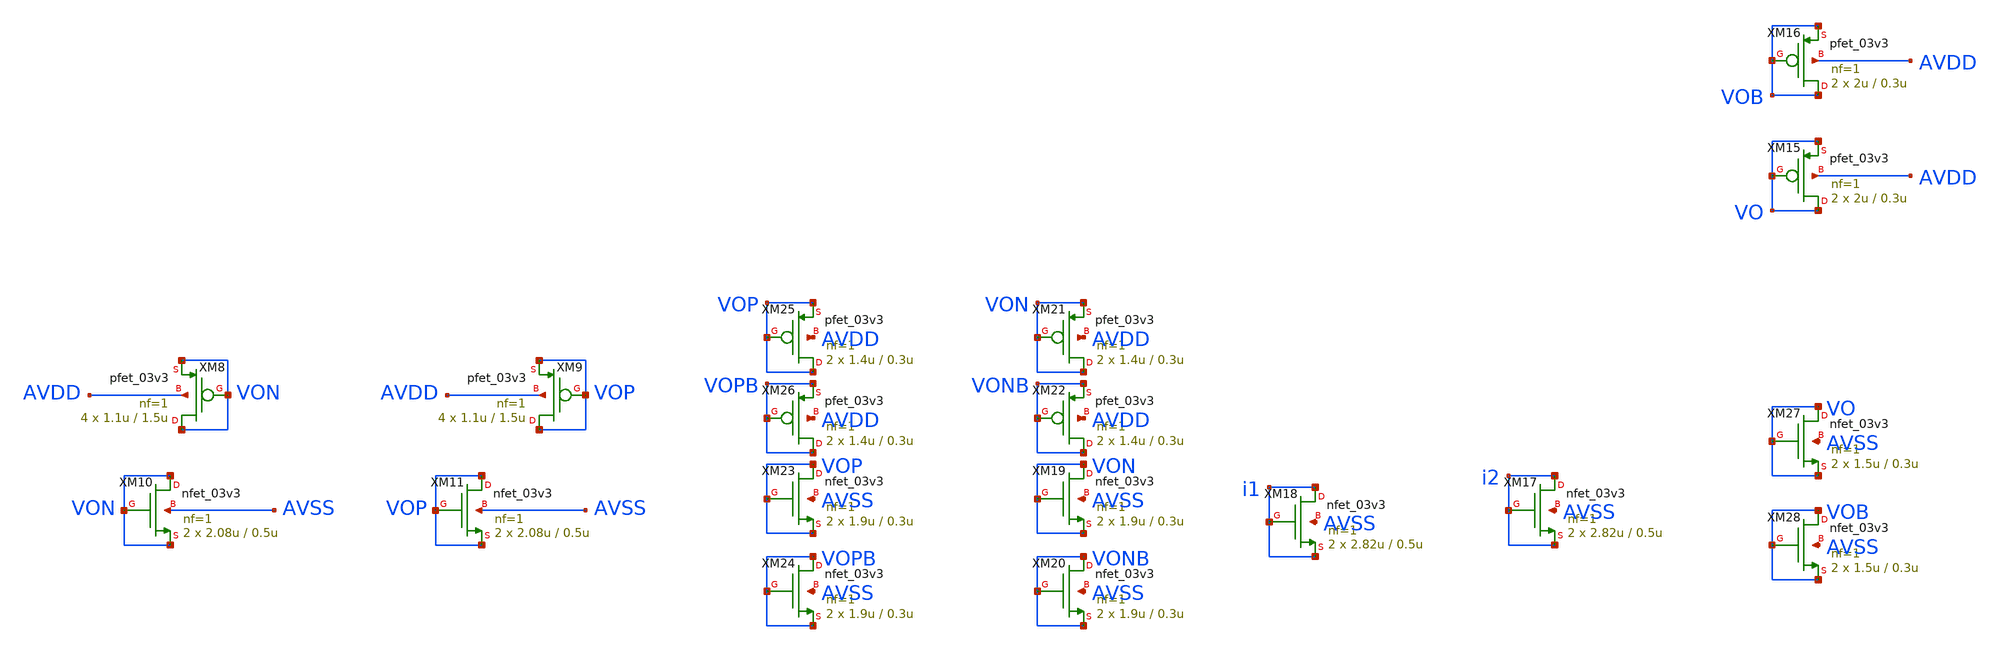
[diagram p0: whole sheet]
** sch_path: designs/untitled-3.sch
**.subckt untitled-3
XM8 VON VON VON AVDD pfet_03v3 L=1.5u W=1.1u nf=1 ad='int((nf+1)/2) * W/nf * 0.18u' as='int((nf+2)/2) * W/nf * 0.18u'
+ pd='2*int((nf+1)/2) * (W/nf + 0.18u)' ps='2*int((nf+2)/2) * (W/nf + 0.18u)' nrd='0.18u / W' nrs='0.18u / W'
+ sa=0 sb=0 sd=0 m=4
XM9 VOP VOP VOP AVDD pfet_03v3 L=1.5u W=1.1u nf=1 ad='int((nf+1)/2) * W/nf * 0.18u' as='int((nf+2)/2) * W/nf * 0.18u'
+ pd='2*int((nf+1)/2) * (W/nf + 0.18u)' ps='2*int((nf+2)/2) * (W/nf + 0.18u)' nrd='0.18u / W' nrs='0.18u / W'
+ sa=0 sb=0 sd=0 m=4
XM10 VON VON VON AVSS nfet_03v3 L=0.5u W=2.08u nf=1 ad='int((nf+1)/2) * W/nf * 0.18u' as='int((nf+2)/2) * W/nf * 0.18u'
+ pd='2*int((nf+1)/2) * (W/nf + 0.18u)' ps='2*int((nf+2)/2) * (W/nf + 0.18u)' nrd='0.18u / W' nrs='0.18u / W'
+ sa=0 sb=0 sd=0 m=2
XM11 VOP VOP VOP AVSS nfet_03v3 L=0.5u W=2.08u nf=1 ad='int((nf+1)/2) * W/nf * 0.18u' as='int((nf+2)/2) * W/nf * 0.18u'
+ pd='2*int((nf+1)/2) * (W/nf + 0.18u)' ps='2*int((nf+2)/2) * (W/nf + 0.18u)' nrd='0.18u / W' nrs='0.18u / W'
+ sa=0 sb=0 sd=0 m=2
XM19 VON VON VON AVSS nfet_03v3 L=0.3u W=1.9u nf=1 ad='int((nf+1)/2) * W/nf * 0.18u' as='int((nf+2)/2) * W/nf * 0.18u'
+ pd='2*int((nf+1)/2) * (W/nf + 0.18u)' ps='2*int((nf+2)/2) * (W/nf + 0.18u)' nrd='0.18u / W' nrs='0.18u / W'
+ sa=0 sb=0 sd=0 m=2
XM20 VONB VONB VONB AVSS nfet_03v3 L=0.3u W=1.9u nf=1 ad='int((nf+1)/2) * W/nf * 0.18u' as='int((nf+2)/2) * W/nf * 0.18u'
+ pd='2*int((nf+1)/2) * (W/nf + 0.18u)' ps='2*int((nf+2)/2) * (W/nf + 0.18u)' nrd='0.18u / W' nrs='0.18u / W'
+ sa=0 sb=0 sd=0 m=2
XM21 VON VON VON AVDD pfet_03v3 L=0.3u W=1.4u nf=1 ad='int((nf+1)/2) * W/nf * 0.18u' as='int((nf+2)/2) * W/nf * 0.18u'
+ pd='2*int((nf+1)/2) * (W/nf + 0.18u)' ps='2*int((nf+2)/2) * (W/nf + 0.18u)' nrd='0.18u / W' nrs='0.18u / W'
+ sa=0 sb=0 sd=0 m=2
XM22 VONB VONB VONB AVDD pfet_03v3 L=0.3u W=1.4u nf=1 ad='int((nf+1)/2) * W/nf * 0.18u' as='int((nf+2)/2) * W/nf * 0.18u'
+ pd='2*int((nf+1)/2) * (W/nf + 0.18u)' ps='2*int((nf+2)/2) * (W/nf + 0.18u)' nrd='0.18u / W' nrs='0.18u / W'
+ sa=0 sb=0 sd=0 m=2
XM23 VOP VOP VOP AVSS nfet_03v3 L=0.3u W=1.9u nf=1 ad='int((nf+1)/2) * W/nf * 0.18u' as='int((nf+2)/2) * W/nf * 0.18u'
+ pd='2*int((nf+1)/2) * (W/nf + 0.18u)' ps='2*int((nf+2)/2) * (W/nf + 0.18u)' nrd='0.18u / W' nrs='0.18u / W'
+ sa=0 sb=0 sd=0 m=2
XM24 VOPB VOPB VOPB AVSS nfet_03v3 L=0.3u W=1.9u nf=1 ad='int((nf+1)/2) * W/nf * 0.18u' as='int((nf+2)/2) * W/nf * 0.18u'
+ pd='2*int((nf+1)/2) * (W/nf + 0.18u)' ps='2*int((nf+2)/2) * (W/nf + 0.18u)' nrd='0.18u / W' nrs='0.18u / W'
+ sa=0 sb=0 sd=0 m=2
XM25 VOP VOP VOP AVDD pfet_03v3 L=0.3u W=1.4u nf=1 ad='int((nf+1)/2) * W/nf * 0.18u' as='int((nf+2)/2) * W/nf * 0.18u'
+ pd='2*int((nf+1)/2) * (W/nf + 0.18u)' ps='2*int((nf+2)/2) * (W/nf + 0.18u)' nrd='0.18u / W' nrs='0.18u / W'
+ sa=0 sb=0 sd=0 m=2
XM26 VOPB VOPB VOPB AVDD pfet_03v3 L=0.3u W=1.4u nf=1 ad='int((nf+1)/2) * W/nf * 0.18u' as='int((nf+2)/2) * W/nf * 0.18u'
+ pd='2*int((nf+1)/2) * (W/nf + 0.18u)' ps='2*int((nf+2)/2) * (W/nf + 0.18u)' nrd='0.18u / W' nrs='0.18u / W'
+ sa=0 sb=0 sd=0 m=2
XM15 VO VO VO AVDD pfet_03v3 L=0.3u W=2u nf=1 ad='int((nf+1)/2) * W/nf * 0.18u' as='int((nf+2)/2) * W/nf * 0.18u'
+ pd='2*int((nf+1)/2) * (W/nf + 0.18u)' ps='2*int((nf+2)/2) * (W/nf + 0.18u)' nrd='0.18u / W' nrs='0.18u / W'
+ sa=0 sb=0 sd=0 m=2
XM16 VOB VOB VOB AVDD pfet_03v3 L=0.3u W=2u nf=1 ad='int((nf+1)/2) * W/nf * 0.18u' as='int((nf+2)/2) * W/nf * 0.18u'
+ pd='2*int((nf+1)/2) * (W/nf + 0.18u)' ps='2*int((nf+2)/2) * (W/nf + 0.18u)' nrd='0.18u / W' nrs='0.18u / W'
+ sa=0 sb=0 sd=0 m=2
XM17 i2 i2 i2 AVSS nfet_03v3 L=0.5u W=2.82u nf=1 ad='int((nf+1)/2) * W/nf * 0.18u' as='int((nf+2)/2) * W/nf * 0.18u'
+ pd='2*int((nf+1)/2) * (W/nf + 0.18u)' ps='2*int((nf+2)/2) * (W/nf + 0.18u)' nrd='0.18u / W' nrs='0.18u / W'
+ sa=0 sb=0 sd=0 m=2
XM18 i1 i1 i1 AVSS nfet_03v3 L=0.5u W=2.82u nf=1 ad='int((nf+1)/2) * W/nf * 0.18u' as='int((nf+2)/2) * W/nf * 0.18u'
+ pd='2*int((nf+1)/2) * (W/nf + 0.18u)' ps='2*int((nf+2)/2) * (W/nf + 0.18u)' nrd='0.18u / W' nrs='0.18u / W'
+ sa=0 sb=0 sd=0 m=2
XM27 VO VO VO AVSS nfet_03v3 L=0.3u W=1.5u nf=1 ad='int((nf+1)/2) * W/nf * 0.18u' as='int((nf+2)/2) * W/nf * 0.18u'
+ pd='2*int((nf+1)/2) * (W/nf + 0.18u)' ps='2*int((nf+2)/2) * (W/nf + 0.18u)' nrd='0.18u / W' nrs='0.18u / W'
+ sa=0 sb=0 sd=0 m=2
XM28 VOB VOB VOB AVSS nfet_03v3 L=0.3u W=1.5u nf=1 ad='int((nf+1)/2) * W/nf * 0.18u' as='int((nf+2)/2) * W/nf * 0.18u'
+ pd='2*int((nf+1)/2) * (W/nf + 0.18u)' ps='2*int((nf+2)/2) * (W/nf + 0.18u)' nrd='0.18u / W' nrs='0.18u / W'
+ sa=0 sb=0 sd=0 m=2
**.ends
.end
